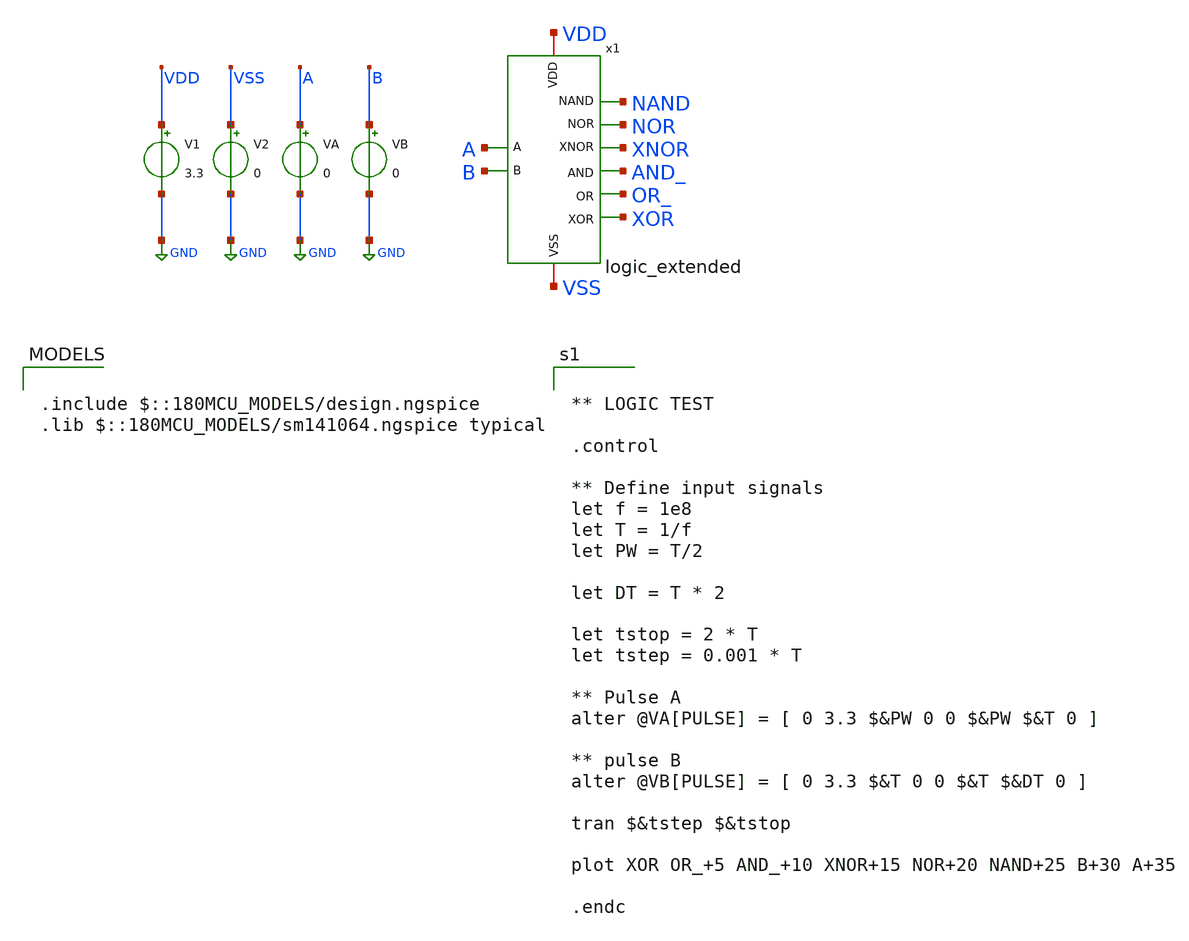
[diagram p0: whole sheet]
** sch_path: CAD4/logic_extended_tb.sch
**.subckt logic_extended_tb
x1 AND_ XOR OR_ NOR VDD VSS XNOR A B NAND logic_extended
V1 VDD GND 3.3
V2 VSS GND 0
VA A GND 0
VB B GND 0
**** begin user architecture code


** LOGIC TEST

.control

** Define input signals
let f = 1e8
let T = 1/f
let PW = T/2

let DT = T * 2

let tstop = 2 * T
let tstep = 0.001 * T

** Pulse A
alter @VA[PULSE] = [ 0 3.3 $&PW 0 0 $&PW $&T 0 ]

** pulse B
alter @VB[PULSE] = [ 0 3.3 $&T 0 0 $&T $&DT 0 ]

tran $&tstep $&tstop

plot XOR OR_+5 AND_+10 XNOR+15 NOR+20 NAND+25 B+30 A+35

.endc



.include $::180MCU_MODELS/design.ngspice
.lib $::180MCU_MODELS/sm141064.ngspice typical

**** end user architecture code
**.ends
.GLOBAL GND
.end
